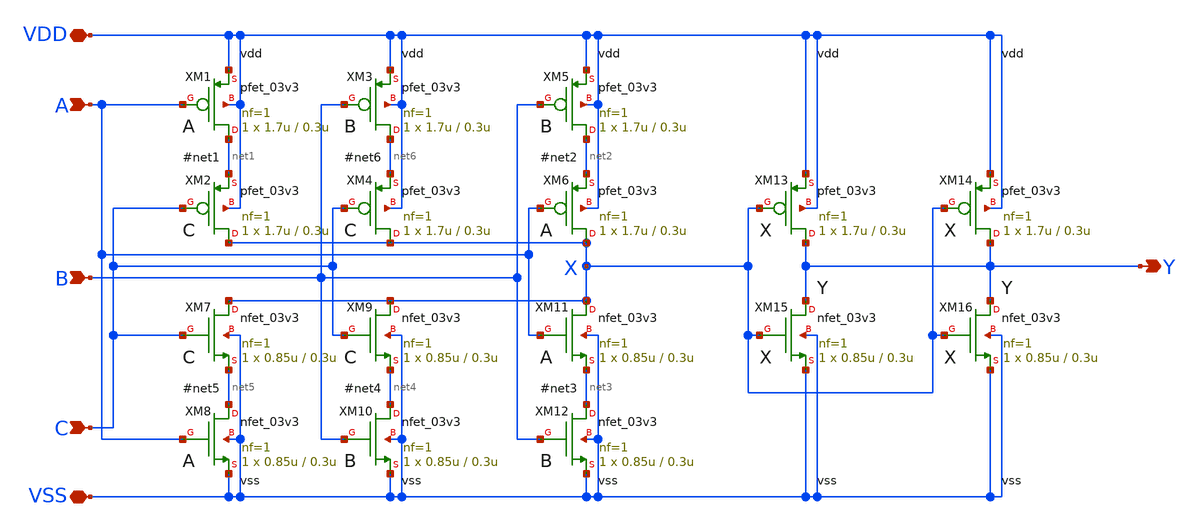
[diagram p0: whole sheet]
** sch_path: xschem/gf180mcu_osu_sc_gp9t3v3__maj3.sch
**.subckt gf180mcu_osu_sc_gp9t3v3__maj3 VDD VSS A B C Y
*.iopin VDD
*.iopin VSS
*.ipin A
*.ipin B
*.ipin C
*.opin Y
XM1 net1 A VDD VDD pfet_03v3 L=0.3u W=1.7u nf=1 ad='int((nf+1)/2) * W/nf * 0.18u' as='int((nf+2)/2) * W/nf * 0.18u'
+ pd='2*int((nf+1)/2) * (W/nf + 0.18u)' ps='2*int((nf+2)/2) * (W/nf + 0.18u)' nrd='0.18u / W' nrs='0.18u / W'
+ sa=0 sb=0 sd=0 m=1
XM2 X C net1 VDD pfet_03v3 L=0.3u W=1.7u nf=1 ad='int((nf+1)/2) * W/nf * 0.18u' as='int((nf+2)/2) * W/nf * 0.18u'
+ pd='2*int((nf+1)/2) * (W/nf + 0.18u)' ps='2*int((nf+2)/2) * (W/nf + 0.18u)' nrd='0.18u / W' nrs='0.18u / W'
+ sa=0 sb=0 sd=0 m=1
XM3 net6 B VDD VDD pfet_03v3 L=0.3u W=1.7u nf=1 ad='int((nf+1)/2) * W/nf * 0.18u' as='int((nf+2)/2) * W/nf * 0.18u'
+ pd='2*int((nf+1)/2) * (W/nf + 0.18u)' ps='2*int((nf+2)/2) * (W/nf + 0.18u)' nrd='0.18u / W' nrs='0.18u / W'
+ sa=0 sb=0 sd=0 m=1
XM5 net2 B VDD VDD pfet_03v3 L=0.3u W=1.7u nf=1 ad='int((nf+1)/2) * W/nf * 0.18u' as='int((nf+2)/2) * W/nf * 0.18u'
+ pd='2*int((nf+1)/2) * (W/nf + 0.18u)' ps='2*int((nf+2)/2) * (W/nf + 0.18u)' nrd='0.18u / W' nrs='0.18u / W'
+ sa=0 sb=0 sd=0 m=1
XM6 X A net2 VDD pfet_03v3 L=0.3u W=1.7u nf=1 ad='int((nf+1)/2) * W/nf * 0.18u' as='int((nf+2)/2) * W/nf * 0.18u'
+ pd='2*int((nf+1)/2) * (W/nf + 0.18u)' ps='2*int((nf+2)/2) * (W/nf + 0.18u)' nrd='0.18u / W' nrs='0.18u / W'
+ sa=0 sb=0 sd=0 m=1
XM4 X C net6 VDD pfet_03v3 L=0.3u W=1.7u nf=1 ad='int((nf+1)/2) * W/nf * 0.18u' as='int((nf+2)/2) * W/nf * 0.18u'
+ pd='2*int((nf+1)/2) * (W/nf + 0.18u)' ps='2*int((nf+2)/2) * (W/nf + 0.18u)' nrd='0.18u / W' nrs='0.18u / W'
+ sa=0 sb=0 sd=0 m=1
XM7 X C net5 VSS nfet_03v3 L=0.3u W=0.85u nf=1 ad='int((nf+1)/2) * W/nf * 0.18u' as='int((nf+2)/2) * W/nf * 0.18u'
+ pd='2*int((nf+1)/2) * (W/nf + 0.18u)' ps='2*int((nf+2)/2) * (W/nf + 0.18u)' nrd='0.18u / W' nrs='0.18u / W'
+ sa=0 sb=0 sd=0 m=1
XM8 net5 A VSS VSS nfet_03v3 L=0.3u W=0.85u nf=1 ad='int((nf+1)/2) * W/nf * 0.18u' as='int((nf+2)/2) * W/nf * 0.18u'
+ pd='2*int((nf+1)/2) * (W/nf + 0.18u)' ps='2*int((nf+2)/2) * (W/nf + 0.18u)' nrd='0.18u / W' nrs='0.18u / W'
+ sa=0 sb=0 sd=0 m=1
XM9 X C net4 VSS nfet_03v3 L=0.3u W=0.85u nf=1 ad='int((nf+1)/2) * W/nf * 0.18u' as='int((nf+2)/2) * W/nf * 0.18u'
+ pd='2*int((nf+1)/2) * (W/nf + 0.18u)' ps='2*int((nf+2)/2) * (W/nf + 0.18u)' nrd='0.18u / W' nrs='0.18u / W'
+ sa=0 sb=0 sd=0 m=1
XM10 net4 B VSS VSS nfet_03v3 L=0.3u W=0.85u nf=1 ad='int((nf+1)/2) * W/nf * 0.18u' as='int((nf+2)/2) * W/nf * 0.18u'
+ pd='2*int((nf+1)/2) * (W/nf + 0.18u)' ps='2*int((nf+2)/2) * (W/nf + 0.18u)' nrd='0.18u / W' nrs='0.18u / W'
+ sa=0 sb=0 sd=0 m=1
XM11 X A net3 VSS nfet_03v3 L=0.3u W=0.85u nf=1 ad='int((nf+1)/2) * W/nf * 0.18u' as='int((nf+2)/2) * W/nf * 0.18u'
+ pd='2*int((nf+1)/2) * (W/nf + 0.18u)' ps='2*int((nf+2)/2) * (W/nf + 0.18u)' nrd='0.18u / W' nrs='0.18u / W'
+ sa=0 sb=0 sd=0 m=1
XM12 net3 B VSS VSS nfet_03v3 L=0.3u W=0.85u nf=1 ad='int((nf+1)/2) * W/nf * 0.18u' as='int((nf+2)/2) * W/nf * 0.18u'
+ pd='2*int((nf+1)/2) * (W/nf + 0.18u)' ps='2*int((nf+2)/2) * (W/nf + 0.18u)' nrd='0.18u / W' nrs='0.18u / W'
+ sa=0 sb=0 sd=0 m=1
XM13 Y X VDD VDD pfet_03v3 L=0.3u W=1.7u nf=1 ad='int((nf+1)/2) * W/nf * 0.18u' as='int((nf+2)/2) * W/nf * 0.18u'
+ pd='2*int((nf+1)/2) * (W/nf + 0.18u)' ps='2*int((nf+2)/2) * (W/nf + 0.18u)' nrd='0.18u / W' nrs='0.18u / W'
+ sa=0 sb=0 sd=0 m=1
XM14 Y X VDD VDD pfet_03v3 L=0.3u W=1.7u nf=1 ad='int((nf+1)/2) * W/nf * 0.18u' as='int((nf+2)/2) * W/nf * 0.18u'
+ pd='2*int((nf+1)/2) * (W/nf + 0.18u)' ps='2*int((nf+2)/2) * (W/nf + 0.18u)' nrd='0.18u / W' nrs='0.18u / W'
+ sa=0 sb=0 sd=0 m=1
XM15 Y X VSS VSS nfet_03v3 L=0.3u W=0.85u nf=1 ad='int((nf+1)/2) * W/nf * 0.18u' as='int((nf+2)/2) * W/nf * 0.18u'
+ pd='2*int((nf+1)/2) * (W/nf + 0.18u)' ps='2*int((nf+2)/2) * (W/nf + 0.18u)' nrd='0.18u / W' nrs='0.18u / W'
+ sa=0 sb=0 sd=0 m=1
XM16 Y X VSS VSS nfet_03v3 L=0.3u W=0.85u nf=1 ad='int((nf+1)/2) * W/nf * 0.18u' as='int((nf+2)/2) * W/nf * 0.18u'
+ pd='2*int((nf+1)/2) * (W/nf + 0.18u)' ps='2*int((nf+2)/2) * (W/nf + 0.18u)' nrd='0.18u / W' nrs='0.18u / W'
+ sa=0 sb=0 sd=0 m=1
**.ends
.end
